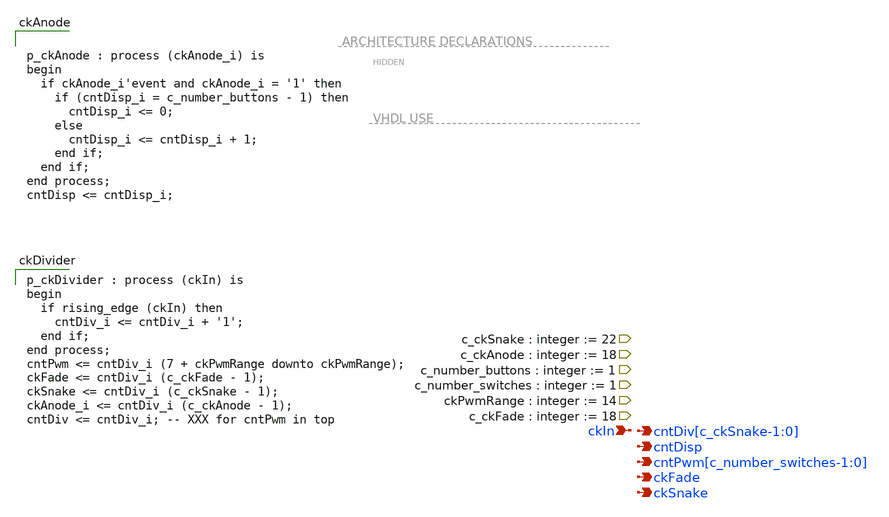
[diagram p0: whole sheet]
** sch_path: xschem/ClkDllDiv16.sch
**.subckt ClkDllDiv16 ckIn cntDisp cntPwm[c_number_switches-1:0] ckFade ckSnake
*+ cntDiv[c_ckSnake-1:0]
*.ipin ckIn
*.opin cntDisp
*.opin cntPwm[c_number_switches-1:0]
*.opin ckFade
*.opin ckSnake
*.opin cntDiv[c_ckSnake-1:0]
**** begin user architecture code

p_ckDivider : process (ckIn) is
begin
  if rising_edge (ckIn) then
    cntDiv_i <= cntDiv_i + '1';
  end if;
end process;
cntPwm <= cntDiv_i (7 + ckPwmRange downto ckPwmRange);
ckFade <= cntDiv_i (c_ckFade - 1);
ckSnake <= cntDiv_i (c_ckSnake - 1);
ckAnode_i <= cntDiv_i (c_ckAnode - 1);
cntDiv <= cntDiv_i; -- XXX for cntPwm in top




p_ckAnode : process (ckAnode_i) is
begin
  if ckAnode_i'event and ckAnode_i = '1' then
    if (cntDisp_i = c_number_buttons - 1) then
      cntDisp_i <= 0;
    else
      cntDisp_i <= cntDisp_i + 1;
    end if;
  end if;
end process;
cntDisp <= cntDisp_i;


**** end user architecture code
**.ends
.end
